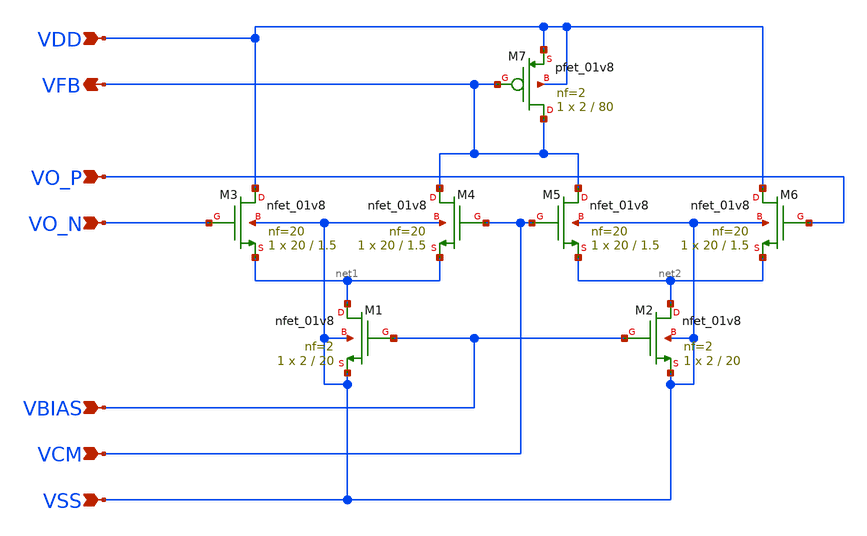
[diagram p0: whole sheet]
** sch_path: circuit-level/xschem/frontend/frontend_cmfb.sch
**.subckt frontend_cmfb VO_P VO_N VDD VSS VBIAS VFB VCM
*.ipin VO_P
*.ipin VO_N
*.ipin VDD
*.ipin VSS
*.ipin VBIAS
*.opin VFB
*.ipin VCM
XM1 net1 VBIAS VSS VSS sky130_fd_pr__nfet_01v8 L=20 W=2 nf=2 ad='int((nf+1)/2) * W/nf * 0.29' as='int((nf+2)/2) * W/nf * 0.29'
+ pd='2*int((nf+1)/2) * (W/nf + 0.29)' ps='2*int((nf+2)/2) * (W/nf + 0.29)' nrd='0.29 / W' nrs='0.29 / W'
+ sa=0 sb=0 sd=0 mult=1 m=1
XM2 net2 VBIAS VSS VSS sky130_fd_pr__nfet_01v8 L=20 W=2 nf=2 ad='int((nf+1)/2) * W/nf * 0.29' as='int((nf+2)/2) * W/nf * 0.29'
+ pd='2*int((nf+1)/2) * (W/nf + 0.29)' ps='2*int((nf+2)/2) * (W/nf + 0.29)' nrd='0.29 / W' nrs='0.29 / W'
+ sa=0 sb=0 sd=0 mult=1 m=1
XM3 VDD VO_N net1 VSS sky130_fd_pr__nfet_01v8 L=1.5 W=20 nf=20 ad='int((nf+1)/2) * W/nf * 0.29' as='int((nf+2)/2) * W/nf * 0.29'
+ pd='2*int((nf+1)/2) * (W/nf + 0.29)' ps='2*int((nf+2)/2) * (W/nf + 0.29)' nrd='0.29 / W' nrs='0.29 / W'
+ sa=0 sb=0 sd=0 mult=1 m=1
XM4 VFB VCM net1 VSS sky130_fd_pr__nfet_01v8 L=1.5 W=20 nf=20 ad='int((nf+1)/2) * W/nf * 0.29' as='int((nf+2)/2) * W/nf * 0.29'
+ pd='2*int((nf+1)/2) * (W/nf + 0.29)' ps='2*int((nf+2)/2) * (W/nf + 0.29)' nrd='0.29 / W' nrs='0.29 / W'
+ sa=0 sb=0 sd=0 mult=1 m=1
XM5 VFB VCM net2 VSS sky130_fd_pr__nfet_01v8 L=1.5 W=20 nf=20 ad='int((nf+1)/2) * W/nf * 0.29' as='int((nf+2)/2) * W/nf * 0.29'
+ pd='2*int((nf+1)/2) * (W/nf + 0.29)' ps='2*int((nf+2)/2) * (W/nf + 0.29)' nrd='0.29 / W' nrs='0.29 / W'
+ sa=0 sb=0 sd=0 mult=1 m=1
XM6 VDD VO_P net2 VSS sky130_fd_pr__nfet_01v8 L=1.5 W=20 nf=20 ad='int((nf+1)/2) * W/nf * 0.29' as='int((nf+2)/2) * W/nf * 0.29'
+ pd='2*int((nf+1)/2) * (W/nf + 0.29)' ps='2*int((nf+2)/2) * (W/nf + 0.29)' nrd='0.29 / W' nrs='0.29 / W'
+ sa=0 sb=0 sd=0 mult=1 m=1
XM7 VFB VFB VDD VDD sky130_fd_pr__pfet_01v8 L=80 W=2 nf=2 ad='int((nf+1)/2) * W/nf * 0.29' as='int((nf+2)/2) * W/nf * 0.29'
+ pd='2*int((nf+1)/2) * (W/nf + 0.29)' ps='2*int((nf+2)/2) * (W/nf + 0.29)' nrd='0.29 / W' nrs='0.29 / W'
+ sa=0 sb=0 sd=0 mult=1 m=1
**.ends
.end
